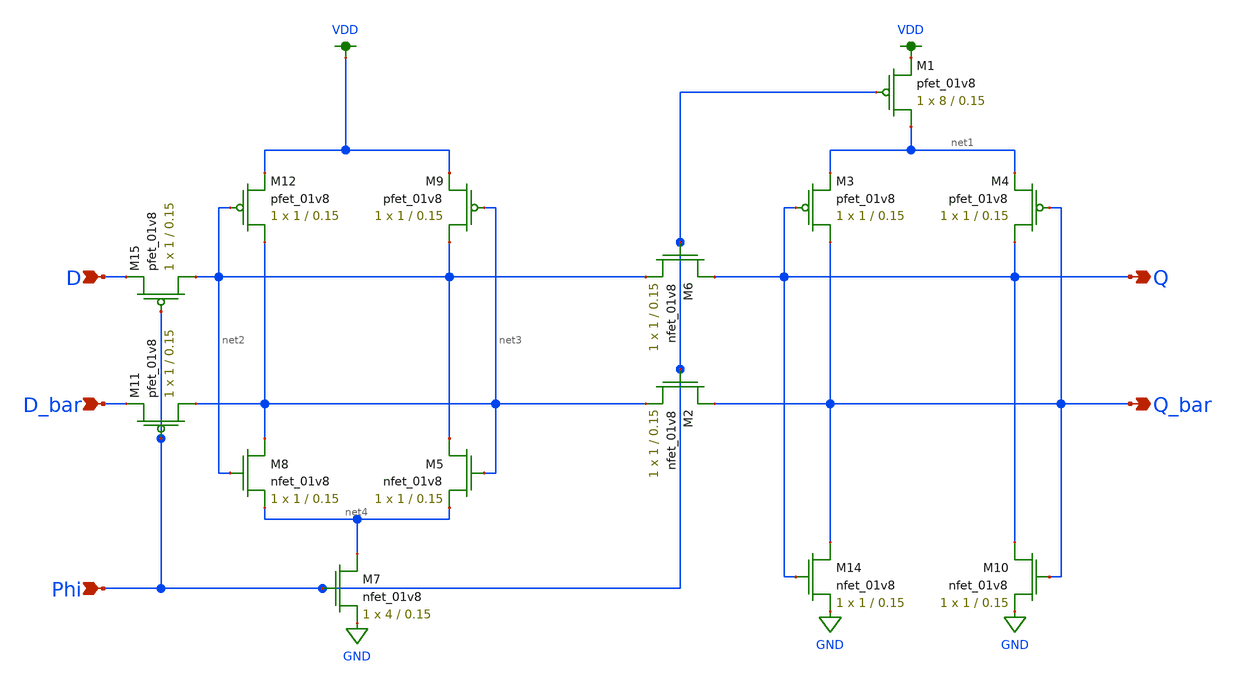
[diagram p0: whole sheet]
** sch_path: schematics/CRSL_edge_sens.sch
**.subckt CRSL_edge_sens D D_bar Q Q_bar Phi
*.ipin D
*.ipin D_bar
*.opin Q
*.opin Q_bar
*.ipin Phi
XM14 Q_bar Q GND GND sky130_fd_pr__nfet_01v8 L=0.15 W=1 nf=1 ad='int((nf+1)/2) * W/nf * 0.29' as='int((nf+2)/2) * W/nf * 0.29'
+ pd='2*int((nf+1)/2) * (W/nf + 0.29)' ps='2*int((nf+2)/2) * (W/nf + 0.29)' nrd='0.29 / W' nrs='0.29 / W'
+ sa=0 sb=0 sd=0 mult=1 m=1
XM2 Q_bar Phi net3 GND sky130_fd_pr__nfet_01v8 L=0.15 W=1 nf=1 ad='int((nf+1)/2) * W/nf * 0.29' as='int((nf+2)/2) * W/nf * 0.29'
+ pd='2*int((nf+1)/2) * (W/nf + 0.29)' ps='2*int((nf+2)/2) * (W/nf + 0.29)' nrd='0.29 / W' nrs='0.29 / W'
+ sa=0 sb=0 sd=0 mult=1 m=1
XM6 Q Phi net2 GND sky130_fd_pr__nfet_01v8 L=0.15 W=1 nf=1 ad='int((nf+1)/2) * W/nf * 0.29' as='int((nf+2)/2) * W/nf * 0.29'
+ pd='2*int((nf+1)/2) * (W/nf + 0.29)' ps='2*int((nf+2)/2) * (W/nf + 0.29)' nrd='0.29 / W' nrs='0.29 / W'
+ sa=0 sb=0 sd=0 mult=1 m=1
XM7 net4 Phi GND GND sky130_fd_pr__nfet_01v8 L=0.15 W=4 nf=1 ad='int((nf+1)/2) * W/nf * 0.29' as='int((nf+2)/2) * W/nf * 0.29'
+ pd='2*int((nf+1)/2) * (W/nf + 0.29)' ps='2*int((nf+2)/2) * (W/nf + 0.29)' nrd='0.29 / W' nrs='0.29 / W'
+ sa=0 sb=0 sd=0 mult=1 m=1
XM8 net3 net2 net4 GND sky130_fd_pr__nfet_01v8 L=0.15 W=1 nf=1 ad='int((nf+1)/2) * W/nf * 0.29' as='int((nf+2)/2) * W/nf * 0.29'
+ pd='2*int((nf+1)/2) * (W/nf + 0.29)' ps='2*int((nf+2)/2) * (W/nf + 0.29)' nrd='0.29 / W' nrs='0.29 / W'
+ sa=0 sb=0 sd=0 mult=1 m=1
XM12 net3 net2 VDD VDD sky130_fd_pr__pfet_01v8 L=0.15 W=1 nf=1 ad='int((nf+1)/2) * W/nf * 0.29' as='int((nf+2)/2) * W/nf * 0.29'
+ pd='2*int((nf+1)/2) * (W/nf + 0.29)' ps='2*int((nf+2)/2) * (W/nf + 0.29)' nrd='0.29 / W' nrs='0.29 / W'
+ sa=0 sb=0 sd=0 mult=1 m=1
XM9 net2 net3 VDD VDD sky130_fd_pr__pfet_01v8 L=0.15 W=1 nf=1 ad='int((nf+1)/2) * W/nf * 0.29' as='int((nf+2)/2) * W/nf * 0.29'
+ pd='2*int((nf+1)/2) * (W/nf + 0.29)' ps='2*int((nf+2)/2) * (W/nf + 0.29)' nrd='0.29 / W' nrs='0.29 / W'
+ sa=0 sb=0 sd=0 mult=1 m=1
XM1 net1 Phi VDD VDD sky130_fd_pr__pfet_01v8 L=0.15 W=8 nf=1 ad='int((nf+1)/2) * W/nf * 0.29' as='int((nf+2)/2) * W/nf * 0.29'
+ pd='2*int((nf+1)/2) * (W/nf + 0.29)' ps='2*int((nf+2)/2) * (W/nf + 0.29)' nrd='0.29 / W' nrs='0.29 / W'
+ sa=0 sb=0 sd=0 mult=1 m=1
XM3 Q_bar Q net1 VDD sky130_fd_pr__pfet_01v8 L=0.15 W=1 nf=1 ad='int((nf+1)/2) * W/nf * 0.29' as='int((nf+2)/2) * W/nf * 0.29'
+ pd='2*int((nf+1)/2) * (W/nf + 0.29)' ps='2*int((nf+2)/2) * (W/nf + 0.29)' nrd='0.29 / W' nrs='0.29 / W'
+ sa=0 sb=0 sd=0 mult=1 m=1
XM4 Q Q_bar net1 VDD sky130_fd_pr__pfet_01v8 L=0.15 W=1 nf=1 ad='int((nf+1)/2) * W/nf * 0.29' as='int((nf+2)/2) * W/nf * 0.29'
+ pd='2*int((nf+1)/2) * (W/nf + 0.29)' ps='2*int((nf+2)/2) * (W/nf + 0.29)' nrd='0.29 / W' nrs='0.29 / W'
+ sa=0 sb=0 sd=0 mult=1 m=1
XM10 Q Q_bar GND GND sky130_fd_pr__nfet_01v8 L=0.15 W=1 nf=1 ad='int((nf+1)/2) * W/nf * 0.29' as='int((nf+2)/2) * W/nf * 0.29'
+ pd='2*int((nf+1)/2) * (W/nf + 0.29)' ps='2*int((nf+2)/2) * (W/nf + 0.29)' nrd='0.29 / W' nrs='0.29 / W'
+ sa=0 sb=0 sd=0 mult=1 m=1
XM5 net2 net3 net4 GND sky130_fd_pr__nfet_01v8 L=0.15 W=1 nf=1 ad='int((nf+1)/2) * W/nf * 0.29' as='int((nf+2)/2) * W/nf * 0.29'
+ pd='2*int((nf+1)/2) * (W/nf + 0.29)' ps='2*int((nf+2)/2) * (W/nf + 0.29)' nrd='0.29 / W' nrs='0.29 / W'
+ sa=0 sb=0 sd=0 mult=1 m=1
XM11 net3 Phi D_bar VDD sky130_fd_pr__pfet_01v8 L=0.15 W=1 nf=1 ad='int((nf+1)/2) * W/nf * 0.29' as='int((nf+2)/2) * W/nf * 0.29'
+ pd='2*int((nf+1)/2) * (W/nf + 0.29)' ps='2*int((nf+2)/2) * (W/nf + 0.29)' nrd='0.29 / W' nrs='0.29 / W'
+ sa=0 sb=0 sd=0 mult=1 m=1
XM15 net2 Phi D VDD sky130_fd_pr__pfet_01v8 L=0.15 W=1 nf=1 ad='int((nf+1)/2) * W/nf * 0.29' as='int((nf+2)/2) * W/nf * 0.29'
+ pd='2*int((nf+1)/2) * (W/nf + 0.29)' ps='2*int((nf+2)/2) * (W/nf + 0.29)' nrd='0.29 / W' nrs='0.29 / W'
+ sa=0 sb=0 sd=0 mult=1 m=1
**.ends
.GLOBAL VDD
.GLOBAL GND
.end
